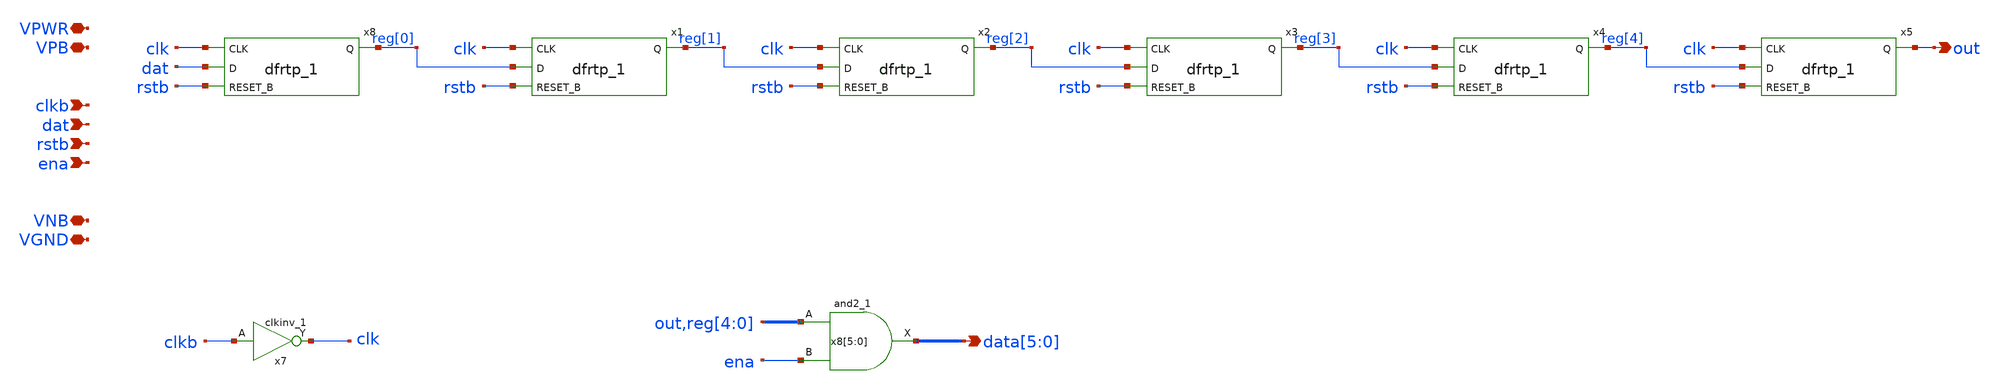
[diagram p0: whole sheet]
** sch_path: tt_um_mosbius/xschem/shift_reg_len6.sch
**.subckt shift_reg_len6 clkb dat rstb VPWR VGND data[5],data[4],data[3],data[2],data[1],data[0] ena
*+ out VPB VNB
*.ipin clkb
*.ipin dat
*.ipin rstb
*.iopin VPWR
*.iopin VGND
*.opin data[5],data[4],data[3],data[2],data[1],data[0]
*.ipin ena
*.opin out
*.iopin VPB
*.iopin VNB
x7 clkb VGND VNB VPB VPWR clk sky130_fd_sc_hd__clkinv_1
x8[5] out ena VGND VNB VPB VPWR data[5] sky130_fd_sc_hd__and2_1
x8[4] reg[4] ena VGND VNB VPB VPWR data[4] sky130_fd_sc_hd__and2_1
x8[3] reg[3] ena VGND VNB VPB VPWR data[3] sky130_fd_sc_hd__and2_1
x8[2] reg[2] ena VGND VNB VPB VPWR data[2] sky130_fd_sc_hd__and2_1
x8[1] reg[1] ena VGND VNB VPB VPWR data[1] sky130_fd_sc_hd__and2_1
x8[0] reg[0] ena VGND VNB VPB VPWR data[0] sky130_fd_sc_hd__and2_1
x8 clk dat rstb VGND VNB VPB VPWR reg[0] sky130_fd_sc_hd__dfrtp_1
x1 clk reg[0] rstb VGND VNB VPB VPWR reg[1] sky130_fd_sc_hd__dfrtp_1
x2 clk reg[1] rstb VGND VNB VPB VPWR reg[2] sky130_fd_sc_hd__dfrtp_1
x3 clk reg[2] rstb VGND VNB VPB VPWR reg[3] sky130_fd_sc_hd__dfrtp_1
x4 clk reg[3] rstb VGND VNB VPB VPWR reg[4] sky130_fd_sc_hd__dfrtp_1
x5 clk reg[4] rstb VGND VNB VPB VPWR out sky130_fd_sc_hd__dfrtp_1
**.ends
.end
